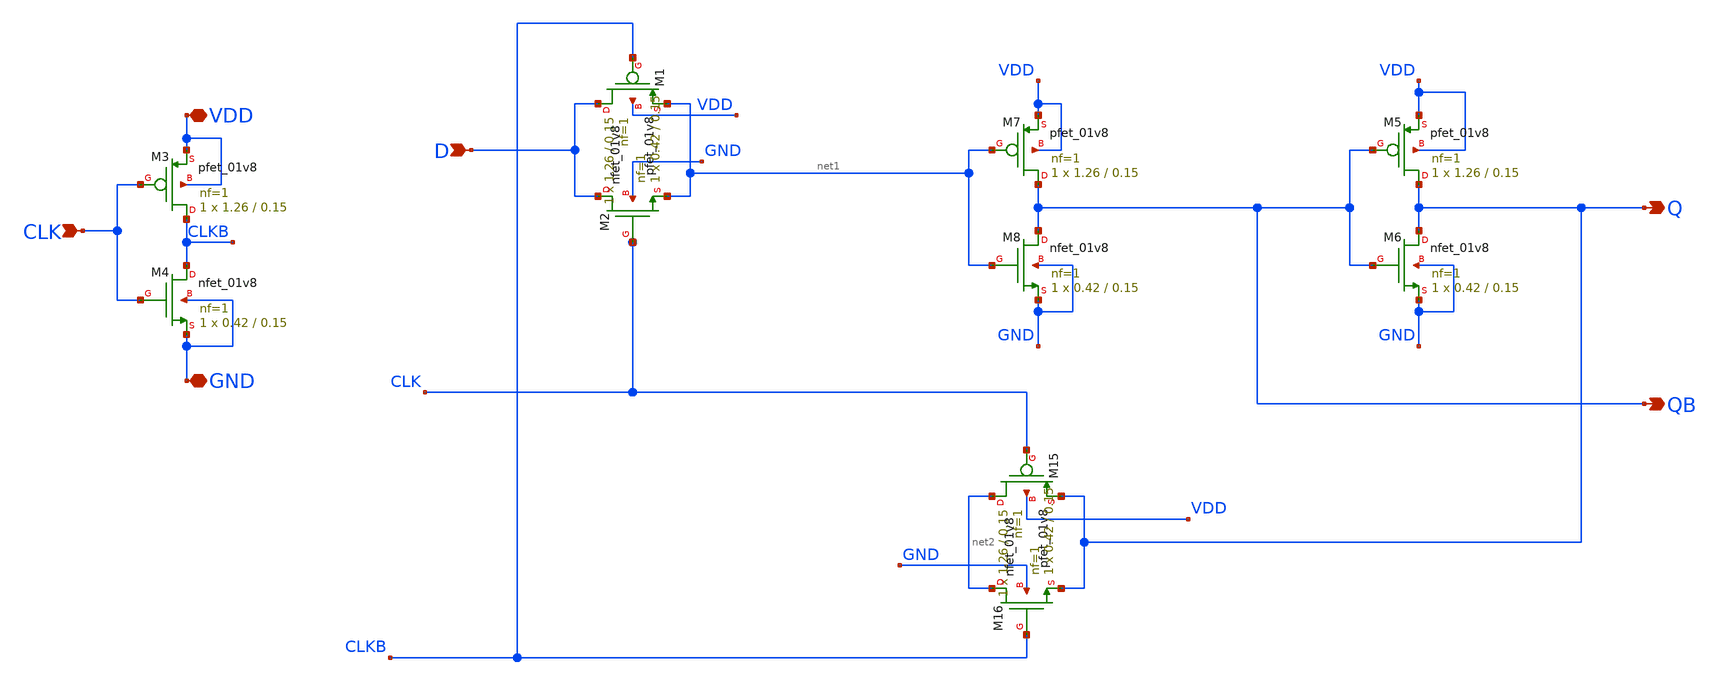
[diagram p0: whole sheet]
** sch_path: cells/DLX1/schematic/dlx1.sch
**.subckt dlx1 D VDD GND CLK QB Q
*.ipin D
*.iopin VDD
*.iopin GND
*.ipin CLK
*.opin QB
*.opin Q
XM1 D CLKB net1 VDD sky130_fd_pr__pfet_01v8 L=0.15 W=1.26 nf=1 ad='int((1 + 1)/2) * 1.26 / 1 * 0.29'
+ as='int((1 + 2)/2) * 1.26 / 1 * 0.29' pd='2*int((1 + 1)/2) * (1.26 / 1 + 0.29)' ps='2*int((1 + 2)/2) * (1.26 / 1 + 0.29)'
+ nrd='0.29 / 1.26 ' nrs='0.29 / 1.26 ' sa=0 sb=0 sd=0 mult=1 m=1
XM2 D CLK net1 GND sky130_fd_pr__nfet_01v8 L=0.15 W=0.42 nf=1 ad='int((1 + 1)/2) * 0.42 / 1 * 0.29' as='int((1 + 2)/2) * 0.42 / 1 * 0.29'
+ pd='2*int((1 + 1)/2) * (0.42 / 1 + 0.29)' ps='2*int((1 + 2)/2) * (0.42 / 1 + 0.29)' nrd='0.29 / 0.42 '
+ nrs='0.29 / 0.42 ' sa=0 sb=0 sd=0 mult=1 m=1
XM5 Q QB VDD VDD sky130_fd_pr__pfet_01v8 L=0.15 W=1.26 nf=1 ad='int((1 + 1)/2) * 1.26 / 1 * 0.29' as='int((1 + 2)/2) * 1.26 / 1 * 0.29'
+ pd='2*int((1 + 1)/2) * (1.26 / 1 + 0.29)' ps='2*int((1 + 2)/2) * (1.26 / 1 + 0.29)' nrd='0.29 / 1.26 '
+ nrs='0.29 / 1.26 ' sa=0 sb=0 sd=0 mult=1 m=1
XM6 Q QB GND GND sky130_fd_pr__nfet_01v8 L=0.15 W=0.42 nf=1 ad='int((1 + 1)/2) * 0.42 / 1 * 0.29' as='int((1 + 2)/2) * 0.42 / 1 * 0.29'
+ pd='2*int((1 + 1)/2) * (0.42 / 1 + 0.29)' ps='2*int((1 + 2)/2) * (0.42 / 1 + 0.29)' nrd='0.29 / 0.42 '
+ nrs='0.29 / 0.42 ' sa=0 sb=0 sd=0 mult=1 m=1
XM7 QB net1 VDD VDD sky130_fd_pr__pfet_01v8 L=0.15 W=1.26 nf=1 ad='int((1 + 1)/2) * 1.26 / 1 * 0.29'
+ as='int((1 + 2)/2) * 1.26 / 1 * 0.29' pd='2*int((1 + 1)/2) * (1.26 / 1 + 0.29)' ps='2*int((1 + 2)/2) * (1.26 / 1 + 0.29)'
+ nrd='0.29 / 1.26 ' nrs='0.29 / 1.26 ' sa=0 sb=0 sd=0 mult=1 m=1
XM8 QB net1 GND GND sky130_fd_pr__nfet_01v8 L=0.15 W=0.42 nf=1 ad='int((1 + 1)/2) * 0.42 / 1 * 0.29'
+ as='int((1 + 2)/2) * 0.42 / 1 * 0.29' pd='2*int((1 + 1)/2) * (0.42 / 1 + 0.29)' ps='2*int((1 + 2)/2) * (0.42 / 1 + 0.29)'
+ nrd='0.29 / 0.42 ' nrs='0.29 / 0.42 ' sa=0 sb=0 sd=0 mult=1 m=1
XM15 net2 CLK Q VDD sky130_fd_pr__pfet_01v8 L=0.15 W=1.26 nf=1 ad='int((1 + 1)/2) * 1.26 / 1 * 0.29'
+ as='int((1 + 2)/2) * 1.26 / 1 * 0.29' pd='2*int((1 + 1)/2) * (1.26 / 1 + 0.29)' ps='2*int((1 + 2)/2) * (1.26 / 1 + 0.29)'
+ nrd='0.29 / 1.26 ' nrs='0.29 / 1.26 ' sa=0 sb=0 sd=0 mult=1 m=1
XM16 net2 CLKB Q GND sky130_fd_pr__nfet_01v8 L=0.15 W=0.42 nf=1 ad='int((1 + 1)/2) * 0.42 / 1 * 0.29'
+ as='int((1 + 2)/2) * 0.42 / 1 * 0.29' pd='2*int((1 + 1)/2) * (0.42 / 1 + 0.29)' ps='2*int((1 + 2)/2) * (0.42 / 1 + 0.29)'
+ nrd='0.29 / 0.42 ' nrs='0.29 / 0.42 ' sa=0 sb=0 sd=0 mult=1 m=1
XM3 CLKB CLK VDD VDD sky130_fd_pr__pfet_01v8 L=0.15 W=1.26 nf=1 ad='int((1 + 1)/2) * 1.26 / 1 * 0.29'
+ as='int((1 + 2)/2) * 1.26 / 1 * 0.29' pd='2*int((1 + 1)/2) * (1.26 / 1 + 0.29)' ps='2*int((1 + 2)/2) * (1.26 / 1 + 0.29)'
+ nrd='0.29 / 1.26 ' nrs='0.29 / 1.26 ' sa=0 sb=0 sd=0 mult=1 m=1
XM4 CLKB CLK GND GND sky130_fd_pr__nfet_01v8 L=0.15 W=0.42 nf=1 ad='int((1 + 1)/2) * 0.42 / 1 * 0.29'
+ as='int((1 + 2)/2) * 0.42 / 1 * 0.29' pd='2*int((1 + 1)/2) * (0.42 / 1 + 0.29)' ps='2*int((1 + 2)/2) * (0.42 / 1 + 0.29)'
+ nrd='0.29 / 0.42 ' nrs='0.29 / 0.42 ' sa=0 sb=0 sd=0 mult=1 m=1
**.ends
.end
